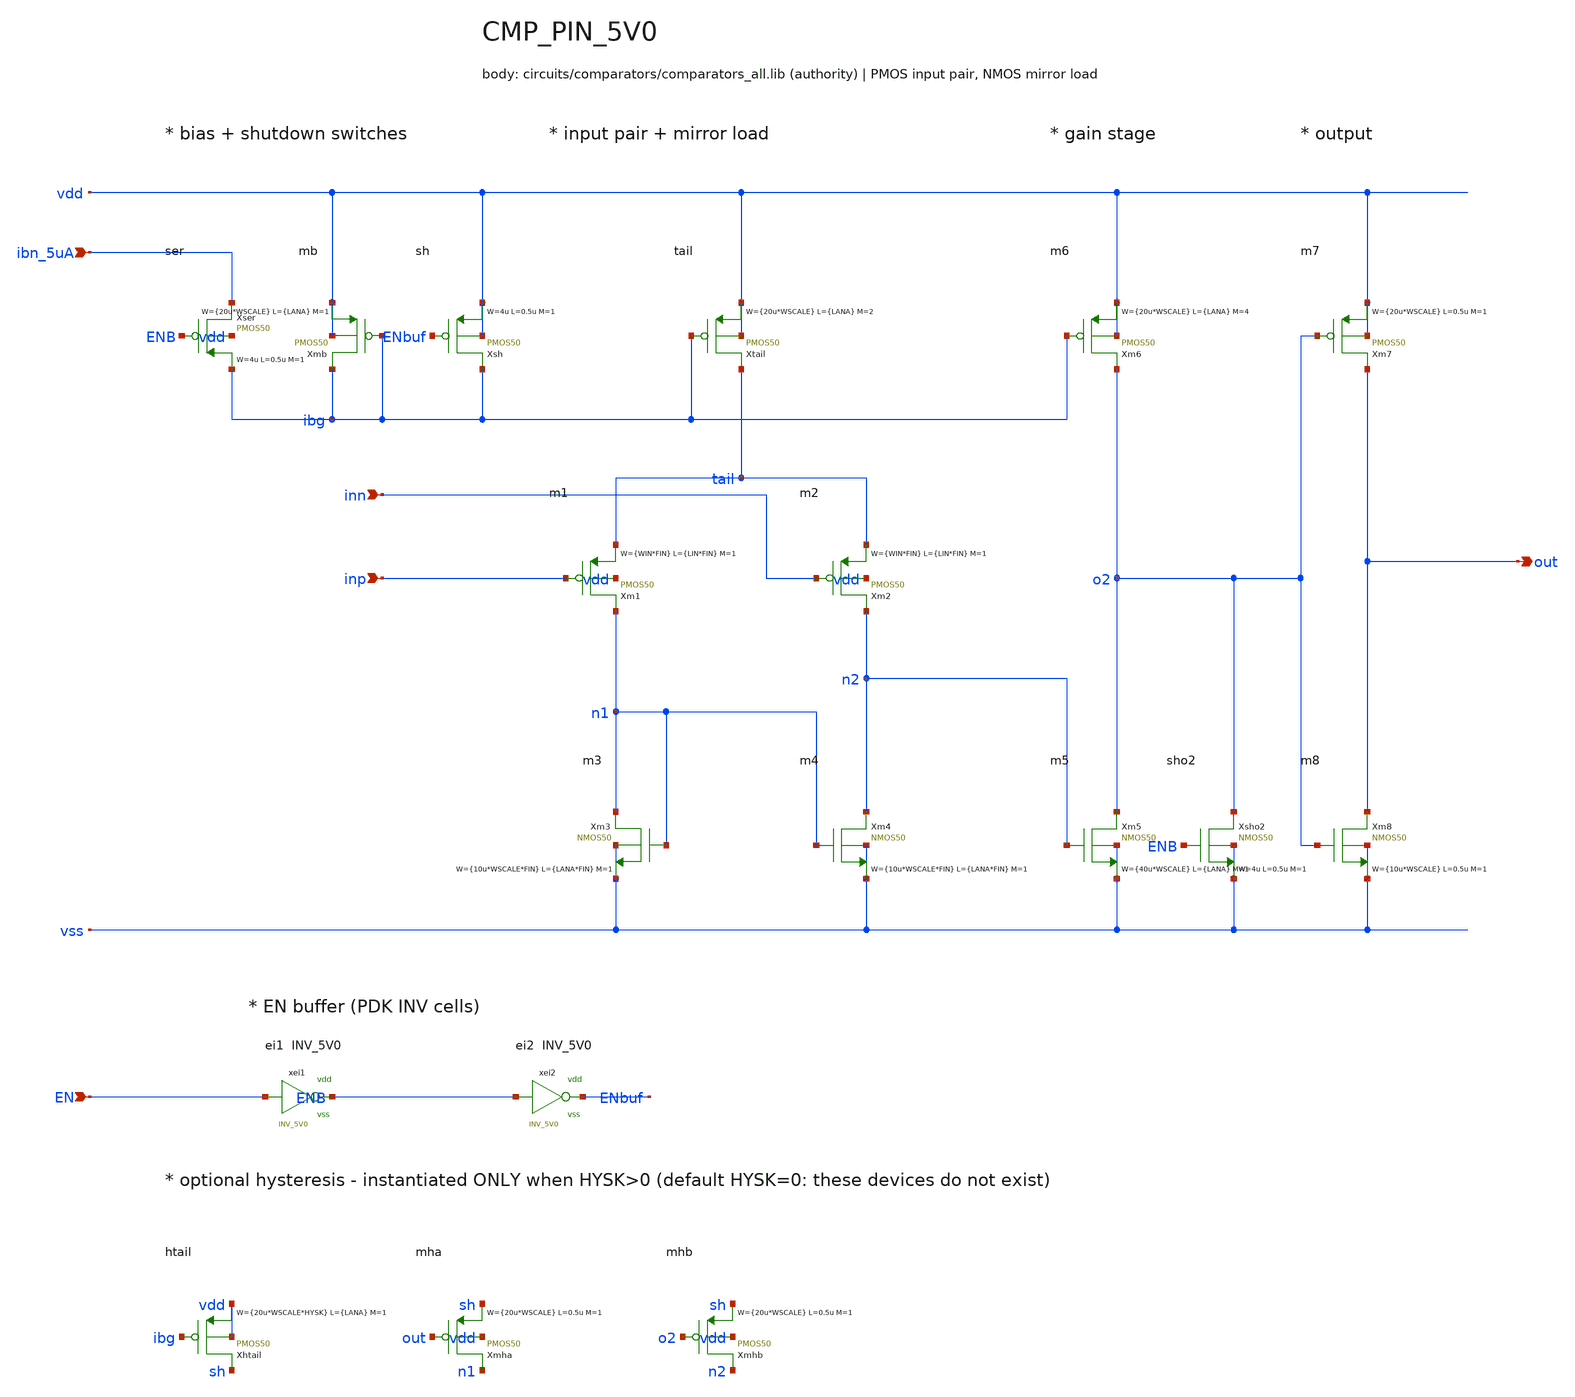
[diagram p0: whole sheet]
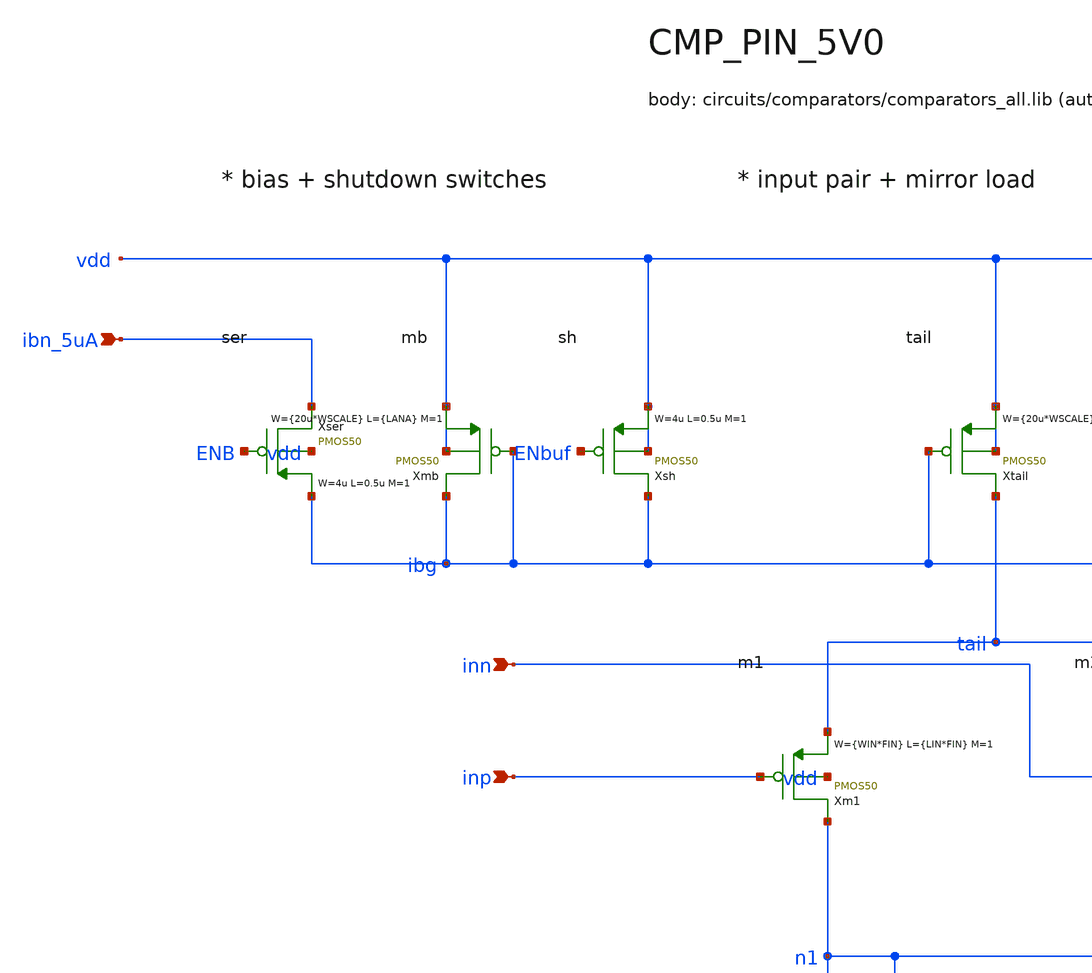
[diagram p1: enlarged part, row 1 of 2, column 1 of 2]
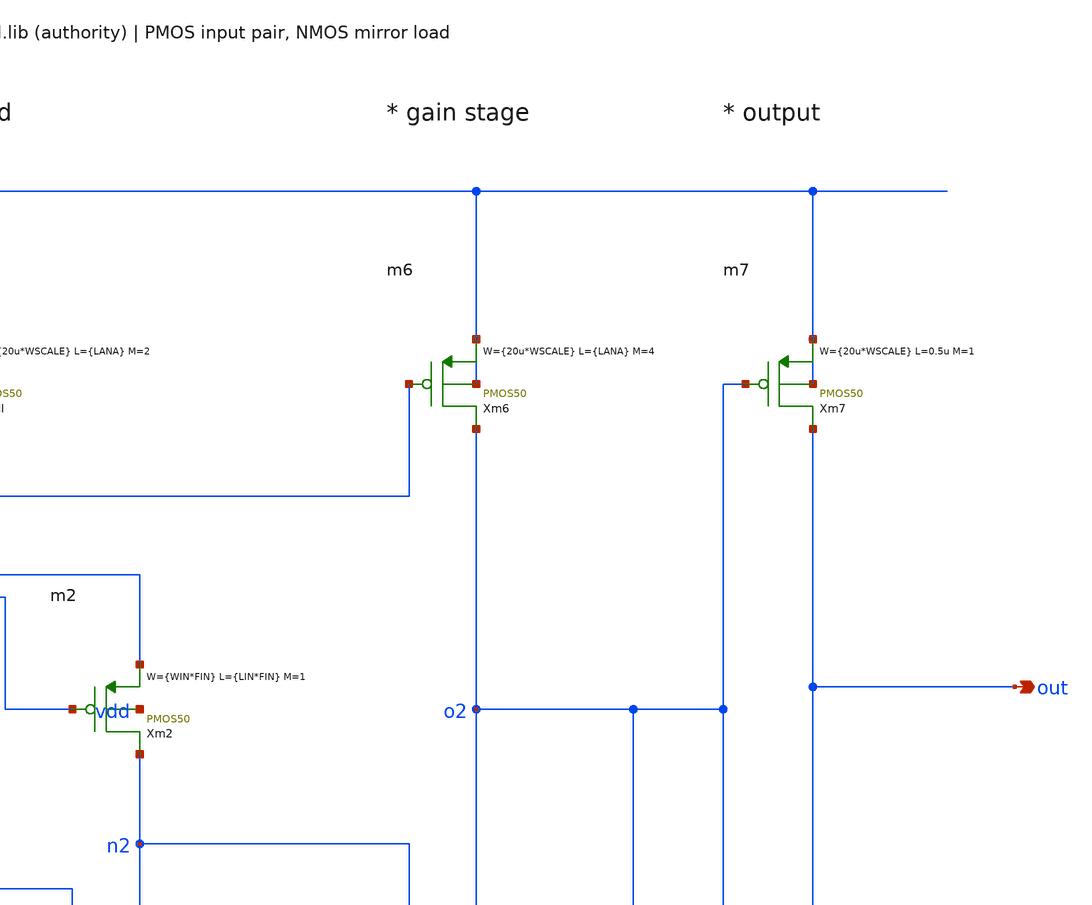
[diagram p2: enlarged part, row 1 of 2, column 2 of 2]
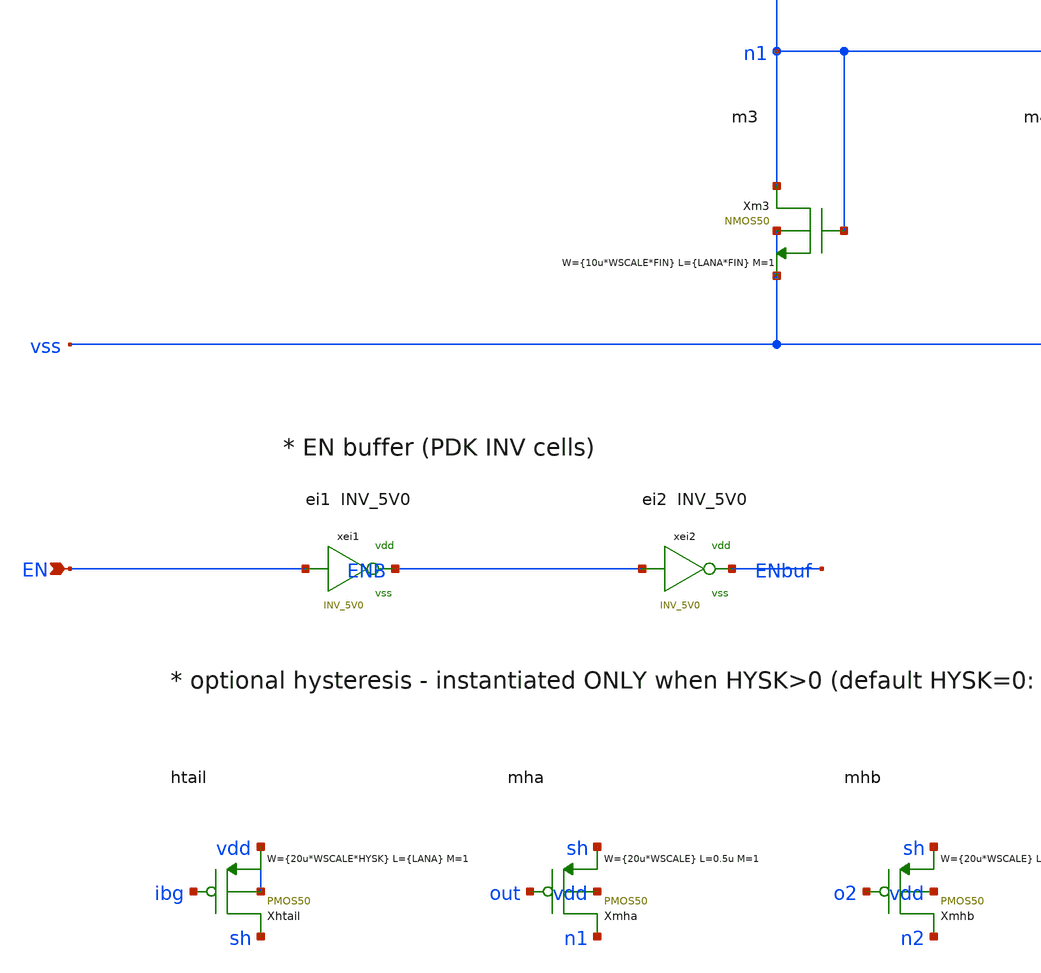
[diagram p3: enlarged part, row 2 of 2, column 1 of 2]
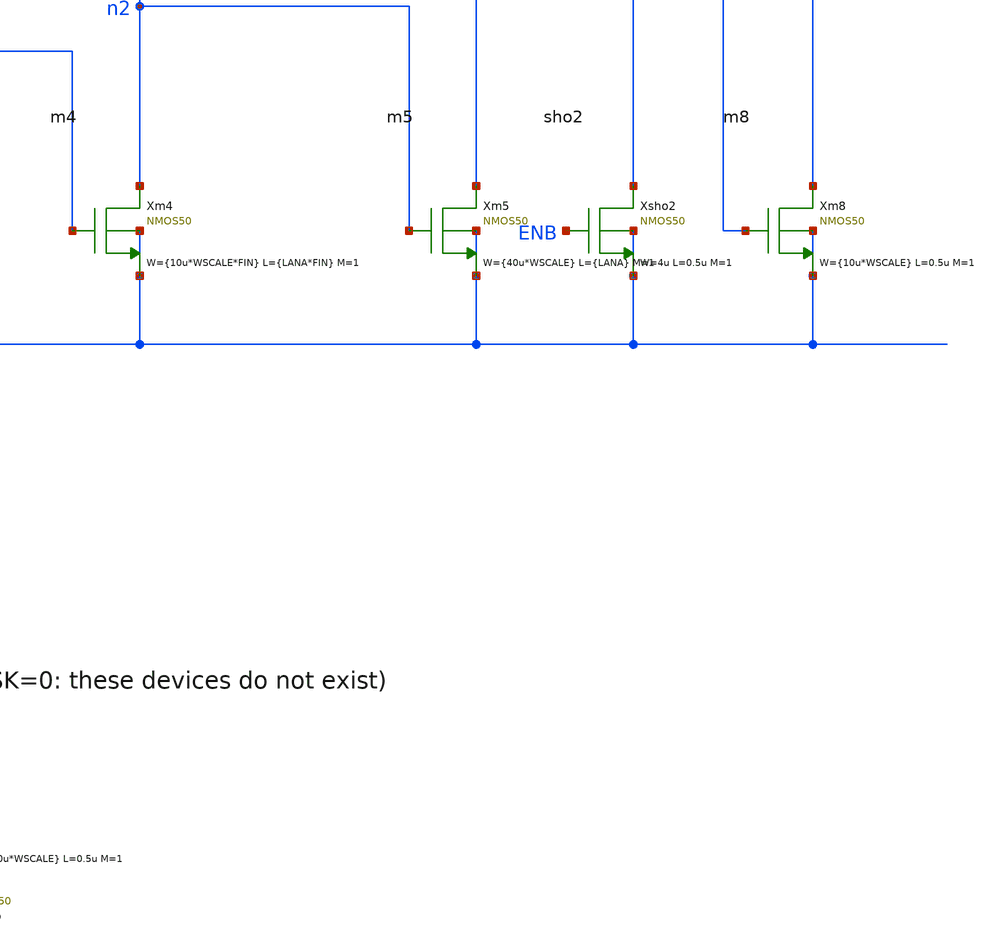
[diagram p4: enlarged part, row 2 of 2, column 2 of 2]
** sch_path: xschem/comparators/CMP_PIN_5V0.sch
**.subckt CMP_PIN_5V0 ibn_5uA out inp inn EN
*.ipin ibn_5uA
*.opin out
*.ipin inp
*.ipin inn
*.ipin EN
Xser ibn_5uA ENB ibg vdd PMOS50 W=4u L=0.5u M=1 MM_SIGMA=0
Xmb ibg ibg vdd vdd PMOS50 W={20u*WSCALE} L={LANA} M=1 MM_SIGMA=0
Xsh ibg ENbuf vdd vdd PMOS50 W=4u L=0.5u M=1 MM_SIGMA=0
Xtail tail ibg vdd vdd PMOS50 W={20u*WSCALE} L={LANA} M=2 MM_SIGMA=0
Xm1 n1 inp tail vdd PMOS50 W={WIN*FIN} L={LIN*FIN} M=1 MM_SIGMA=0
Xm2 n2 inn tail vdd PMOS50 W={WIN*FIN} L={LIN*FIN} M=1 MM_SIGMA=0
Xm3 n1 n1 vss vss NMOS50 W={10u*WSCALE*FIN} L={LANA*FIN} M=1 MM_SIGMA=0
Xm4 n2 n1 vss vss NMOS50 W={10u*WSCALE*FIN} L={LANA*FIN} M=1 MM_SIGMA=0
Xm5 o2 n2 vss vss NMOS50 W={40u*WSCALE} L={LANA} M=1 MM_SIGMA=0
Xm6 o2 ibg vdd vdd PMOS50 W={20u*WSCALE} L={LANA} M=4 MM_SIGMA=0
Xm7 out o2 vdd vdd PMOS50 W={20u*WSCALE} L=0.5u M=1 MM_SIGMA=0
Xm8 out o2 vss vss NMOS50 W={10u*WSCALE} L=0.5u M=1 MM_SIGMA=0
Xsho2 o2 ENB vss vss NMOS50 W=4u L=0.5u M=1 MM_SIGMA=0
xei1 EN ENB vdd vss INV_5V0
xei2 ENB ENbuf vdd vss INV_5V0
Xhtail sh ibg vdd vdd PMOS50 W={20u*WSCALE*HYSK} L={LANA} M=1 MM_SIGMA=0
Xmha n1 out sh vdd PMOS50 W={20u*WSCALE} L=0.5u M=1 MM_SIGMA=0
Xmhb n2 o2 sh vdd PMOS50 W={20u*WSCALE} L=0.5u M=1 MM_SIGMA=0
**.ends

* expanding   symbol:  logic/INV_5V0.sym # of pins=2
** sym_path: xschem/logic/INV_5V0.sym
* INV_5V0 body is defined in circuits/async_logic_design/cells.lib
.end
